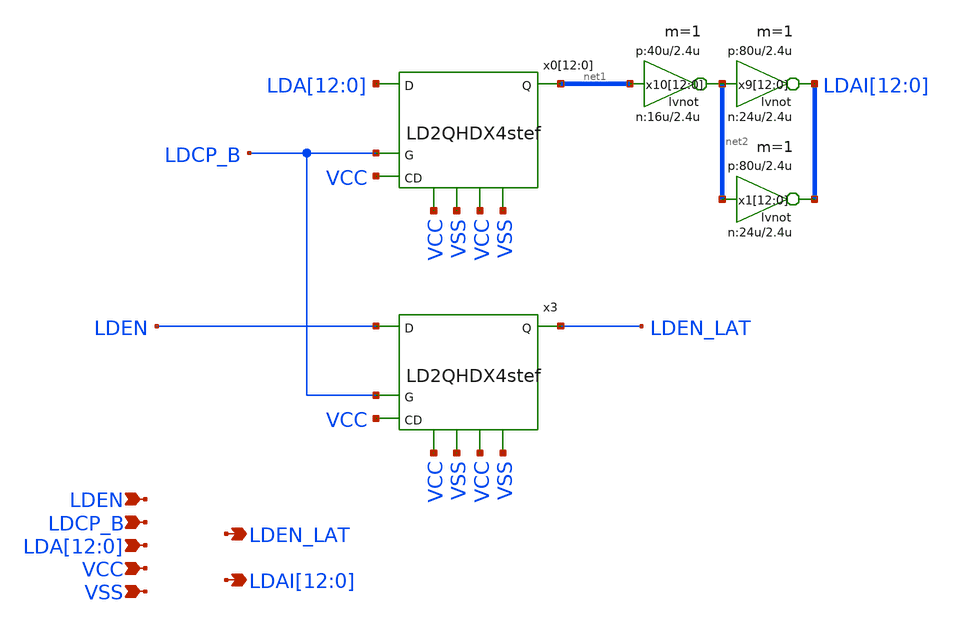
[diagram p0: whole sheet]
** sch_path: xschem-src/xschem_library/rom8k/rom2_addlatch.sch
* Copyright (C) 1998-2026 Stefan Frederik Schippers
* This program is free software; you can redistribute it and/or modify
* it under the terms of the GNU General Public License as published by
* the Free Software Foundation; either version 2 of the License, or
* (at your option) any later version.
* This program is distributed in the hope that it will be useful,
* but WITHOUT ANY WARRANTY; without even the implied warranty of
* MERCHANTABILITY or FITNESS FOR A PARTICULAR PURPOSE.  See the
* GNU General Public License for more details.
* You should have received a copy of the GNU General Public License
* along with this program; if not, write to the Free Software
**.subckt rom2_addlatch LDEN_LAT
*+ LDAI[12],LDAI[11],LDAI[10],LDAI[9],LDAI[8],LDAI[7],LDAI[6],LDAI[5],LDAI[4],LDAI[3],LDAI[2],LDAI[1],LDAI[0] LDEN LDCP_B
*+ LDA[12],LDA[11],LDA[10],LDA[9],LDA[8],LDA[7],LDA[6],LDA[5],LDA[4],LDA[3],LDA[2],LDA[1],LDA[0] VCC VSS
*.opin LDEN_LAT
*.opin
*+ LDAI[12],LDAI[11],LDAI[10],LDAI[9],LDAI[8],LDAI[7],LDAI[6],LDAI[5],LDAI[4],LDAI[3],LDAI[2],LDAI[1],LDAI[0]
*.ipin LDEN
*.ipin LDCP_B
*.ipin LDA[12],LDA[11],LDA[10],LDA[9],LDA[8],LDA[7],LDA[6],LDA[5],LDA[4],LDA[3],LDA[2],LDA[1],LDA[0]
*.ipin VCC
*.ipin VSS
x0[12] LDA[12] LDCP_B VCC net1[12] VCC VSS VCC VSS LD2QHDX4stef
x0[11] LDA[11] LDCP_B VCC net1[11] VCC VSS VCC VSS LD2QHDX4stef
x0[10] LDA[10] LDCP_B VCC net1[10] VCC VSS VCC VSS LD2QHDX4stef
x0[9] LDA[9] LDCP_B VCC net1[9] VCC VSS VCC VSS LD2QHDX4stef
x0[8] LDA[8] LDCP_B VCC net1[8] VCC VSS VCC VSS LD2QHDX4stef
x0[7] LDA[7] LDCP_B VCC net1[7] VCC VSS VCC VSS LD2QHDX4stef
x0[6] LDA[6] LDCP_B VCC net1[6] VCC VSS VCC VSS LD2QHDX4stef
x0[5] LDA[5] LDCP_B VCC net1[5] VCC VSS VCC VSS LD2QHDX4stef
x0[4] LDA[4] LDCP_B VCC net1[4] VCC VSS VCC VSS LD2QHDX4stef
x0[3] LDA[3] LDCP_B VCC net1[3] VCC VSS VCC VSS LD2QHDX4stef
x0[2] LDA[2] LDCP_B VCC net1[2] VCC VSS VCC VSS LD2QHDX4stef
x0[1] LDA[1] LDCP_B VCC net1[1] VCC VSS VCC VSS LD2QHDX4stef
x0[0] LDA[0] LDCP_B VCC net1[0] VCC VSS VCC VSS LD2QHDX4stef
x9[12] LDAI[12] net2[12] vcc vss lvnot wn=24u lln=2.4u wp=80u lp=2.4u m=1
x9[11] LDAI[11] net2[11] vcc vss lvnot wn=24u lln=2.4u wp=80u lp=2.4u m=1
x9[10] LDAI[10] net2[10] vcc vss lvnot wn=24u lln=2.4u wp=80u lp=2.4u m=1
x9[9] LDAI[9] net2[9] vcc vss lvnot wn=24u lln=2.4u wp=80u lp=2.4u m=1
x9[8] LDAI[8] net2[8] vcc vss lvnot wn=24u lln=2.4u wp=80u lp=2.4u m=1
x9[7] LDAI[7] net2[7] vcc vss lvnot wn=24u lln=2.4u wp=80u lp=2.4u m=1
x9[6] LDAI[6] net2[6] vcc vss lvnot wn=24u lln=2.4u wp=80u lp=2.4u m=1
x9[5] LDAI[5] net2[5] vcc vss lvnot wn=24u lln=2.4u wp=80u lp=2.4u m=1
x9[4] LDAI[4] net2[4] vcc vss lvnot wn=24u lln=2.4u wp=80u lp=2.4u m=1
x9[3] LDAI[3] net2[3] vcc vss lvnot wn=24u lln=2.4u wp=80u lp=2.4u m=1
x9[2] LDAI[2] net2[2] vcc vss lvnot wn=24u lln=2.4u wp=80u lp=2.4u m=1
x9[1] LDAI[1] net2[1] vcc vss lvnot wn=24u lln=2.4u wp=80u lp=2.4u m=1
x9[0] LDAI[0] net2[0] vcc vss lvnot wn=24u lln=2.4u wp=80u lp=2.4u m=1
x10[12] net2[12] net1[12] vcc vss lvnot wn=16u lln=2.4u wp=40u lp=2.4u m=1
x10[11] net2[11] net1[11] vcc vss lvnot wn=16u lln=2.4u wp=40u lp=2.4u m=1
x10[10] net2[10] net1[10] vcc vss lvnot wn=16u lln=2.4u wp=40u lp=2.4u m=1
x10[9] net2[9] net1[9] vcc vss lvnot wn=16u lln=2.4u wp=40u lp=2.4u m=1
x10[8] net2[8] net1[8] vcc vss lvnot wn=16u lln=2.4u wp=40u lp=2.4u m=1
x10[7] net2[7] net1[7] vcc vss lvnot wn=16u lln=2.4u wp=40u lp=2.4u m=1
x10[6] net2[6] net1[6] vcc vss lvnot wn=16u lln=2.4u wp=40u lp=2.4u m=1
x10[5] net2[5] net1[5] vcc vss lvnot wn=16u lln=2.4u wp=40u lp=2.4u m=1
x10[4] net2[4] net1[4] vcc vss lvnot wn=16u lln=2.4u wp=40u lp=2.4u m=1
x10[3] net2[3] net1[3] vcc vss lvnot wn=16u lln=2.4u wp=40u lp=2.4u m=1
x10[2] net2[2] net1[2] vcc vss lvnot wn=16u lln=2.4u wp=40u lp=2.4u m=1
x10[1] net2[1] net1[1] vcc vss lvnot wn=16u lln=2.4u wp=40u lp=2.4u m=1
x10[0] net2[0] net1[0] vcc vss lvnot wn=16u lln=2.4u wp=40u lp=2.4u m=1
x3 LDEN LDCP_B VCC LDEN_LAT VCC VSS VCC VSS LD2QHDX4stef
x1[12] LDAI[12] net2[12] vcc vss lvnot wn=24u lln=2.4u wp=80u lp=2.4u m=1
x1[11] LDAI[11] net2[11] vcc vss lvnot wn=24u lln=2.4u wp=80u lp=2.4u m=1
x1[10] LDAI[10] net2[10] vcc vss lvnot wn=24u lln=2.4u wp=80u lp=2.4u m=1
x1[9] LDAI[9] net2[9] vcc vss lvnot wn=24u lln=2.4u wp=80u lp=2.4u m=1
x1[8] LDAI[8] net2[8] vcc vss lvnot wn=24u lln=2.4u wp=80u lp=2.4u m=1
x1[7] LDAI[7] net2[7] vcc vss lvnot wn=24u lln=2.4u wp=80u lp=2.4u m=1
x1[6] LDAI[6] net2[6] vcc vss lvnot wn=24u lln=2.4u wp=80u lp=2.4u m=1
x1[5] LDAI[5] net2[5] vcc vss lvnot wn=24u lln=2.4u wp=80u lp=2.4u m=1
x1[4] LDAI[4] net2[4] vcc vss lvnot wn=24u lln=2.4u wp=80u lp=2.4u m=1
x1[3] LDAI[3] net2[3] vcc vss lvnot wn=24u lln=2.4u wp=80u lp=2.4u m=1
x1[2] LDAI[2] net2[2] vcc vss lvnot wn=24u lln=2.4u wp=80u lp=2.4u m=1
x1[1] LDAI[1] net2[1] vcc vss lvnot wn=24u lln=2.4u wp=80u lp=2.4u m=1
x1[0] LDAI[0] net2[0] vcc vss lvnot wn=24u lln=2.4u wp=80u lp=2.4u m=1
**.ends

* expanding   symbol:  LD2QHDX4stef.sym # of pins=8
** sym_path: xschem-src/xschem_library/rom8k/LD2QHDX4stef.sym
** sch_path: xschem-src/xschem_library/rom8k/LD2QHDX4stef.sch
.subckt LD2QHDX4stef D G CD Q vcc vss vccsup vsssup
*.ipin D
*.ipin G
*.ipin CD
*.opin Q
*.iopin vcc
*.iopin vss
*.iopin vccsup
*.iopin vsssup
c2 BN vss 3f m=1
c3 DDN vss 5f m=1
c5 GN vss 5f m=1
c7 FN vss 3f m=1
x8 DDN BN G GN vccsup vsssup passhs WN=12u LN=1.2u WP=12u LP=1.2u
m17 DDN D net2 vsssup cmosn w=8.4u l=2.4u ad={8.4u *2.2u} as={8.4u *2.2u} pd={8.4u *2+4.4u} ps={8.4u *2+4.4u}
+ m=1
m1 DDN D net3 vccsup cmosp w=20u l=2.4u ad={20u *2.2u} as={20u *2.2u} pd={20u *2+4.4u} ps={20u *2+4.4u}
+ m=1
m2 net2 G net1 vsssup cmosn w=8.4u l=2.4u ad={8.4u *2.2u} as={8.4u *2.2u} pd={8.4u *2+4.4u} ps={8.4u *2+4.4u}
+ m=1
m3 net3 GN vcc vccsup cmosp w=20u l=2.4u ad={20u *2.2u} as={20u *2.2u} pd={20u *2+4.4u} ps={20u *2+4.4u}
+ m=1
m4 BN FN net1 vsssup cmosn w=8.4u l=2.4u ad={8.4u *2.2u} as={8.4u *2.2u} pd={8.4u *2+4.4u} ps={8.4u *2+4.4u}
+ m=1
m5 BN FN vcc vccsup cmosp w=8.4u l=2.4u ad={8.4u *2.2u} as={8.4u *2.2u} pd={8.4u *2+4.4u} ps={8.4u *2+4.4u}
+ m=1
m8 net1 CD vss vsssup cmosn w=24u l=2.4u ad={24u *2.2u} as={24u *2.2u} pd={24u *2+4.4u} ps={24u *2+4.4u}
+ m=1
m11 DDN CD vcc vccsup cmosp w=8.4u l=2.4u ad={8.4u *2.2u} as={8.4u *2.2u} pd={8.4u *2+4.4u} ps={8.4u *2+4.4u}
+ m=1
x10 FN DDN vcc vss lvnot wn=8.4u lln=2.4u wp=8.4u lp=2.4u m=1
x1 GN G vcc vss lvnot wn=40u lln=2.4u wp=40u lp=2.4u m=1
x2 Q DDN vcc vss lvnot wn=40u lln=2.4u wp=100u lp=2.4u m=1
.save v(ddn)
.save v(fn)
.ends


* expanding   symbol:  lvnot.sym # of pins=2
** sym_path: xschem-src/xschem_library/rom8k/lvnot.sym
** sch_path: xschem-src/xschem_library/rom8k/lvnot.sch
.subckt lvnot y a VCCPIN VSSPIN     wn=10u lln=1.2u wp=10u lp=1.2u
*.opin y
*.ipin a
m2 DP a VCCPIN VCCPIN cmosp w=wp l=lp ad='wp *4.6u' as='wp *4.6u' pd='wp *2+9.2u' ps='wp *2+9.2u' m=1
m1 DN a VSSPIN VSSPIN cmosn w=wn l=lln ad='wn *4.3u' as='wn *4.3u' pd='wn *2+8.6u' ps='wn *2+8.6u' m=1
Vmeas DP y 0
.save i(vmeas)
Vmeas1 y DN 0
.save i(vmeas1)
.save v(dp)
.save v(dn)
.ends


* expanding   symbol:  passhs.sym # of pins=4
** sym_path: xschem-src/xschem_library/rom8k/passhs.sym
** sch_path: xschem-src/xschem_library/rom8k/passhs.sch
.subckt passhs Z A EN E VCCPIN VSSPIN  WN=2u LN=1.2u WP=2u LP=1.2u
*.iopin Z
*.iopin A
*.ipin EN
*.ipin E
m60 Z EN A VCCPIN cmosp w=WP l=2.4u ad='WP *4.6u' as='WP *4.6u' pd='WP *2+9.2u' ps='WP *2+9.2u' m=1
m1 A E Z VSSPIN cmosn w=WN l=2.4u ad='WN *4.3u' as='WN *4.3u' pd='WN *2+8.6u' ps='WN *2+8.6u' m=1
* noconn VSSPIN
* noconn VCCPIN
.ends

.end
